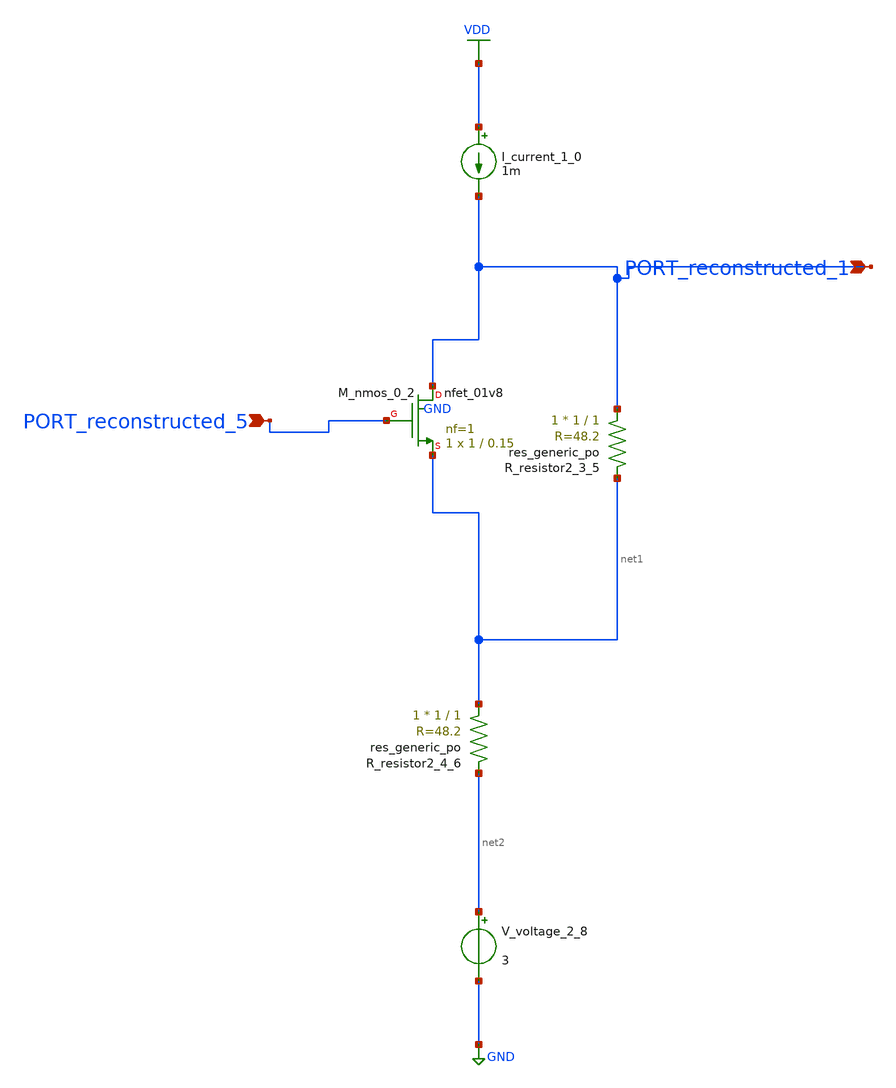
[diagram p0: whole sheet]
** sch_path: schematics/AMSNet/121.sch
**.subckt 121 PORT_reconstructed_5 PORT_reconstructed_1
*.ipin PORT_reconstructed_5
*.ipin PORT_reconstructed_1
I_current_1_0 VDD PORT_reconstructed_1 1m
XM_nmos_0_2 PORT_reconstructed_1 PORT_reconstructed_5 net1 GND sky130_fd_pr__nfet_01v8 L=0.15 W=1 nf=1
+ ad='int((1 + 1)/2) * 1 / 1 * 0.29' as='int((1 + 2)/2) * 1 / 1 * 0.29' pd='2*int((1 + 1)/2) * (1 / 1 + 0.29)'
+ ps='2*int((1 + 2)/2) * (1 / 1 + 0.29)' nrd='0.29 / 1 ' nrs='0.29 / 1 ' sa=0 sb=0 sd=0 mult=1 m=1
XR_resistor2_3_5 PORT_reconstructed_1 net1 sky130_fd_pr__res_generic_po W=1 L=1 m=1
XR_resistor2_4_6 net1 net2 sky130_fd_pr__res_generic_po W=1 L=1 m=1
V_voltage_2_8 net2 GND 3
**.ends
.GLOBAL GND
.GLOBAL VDD
.end
